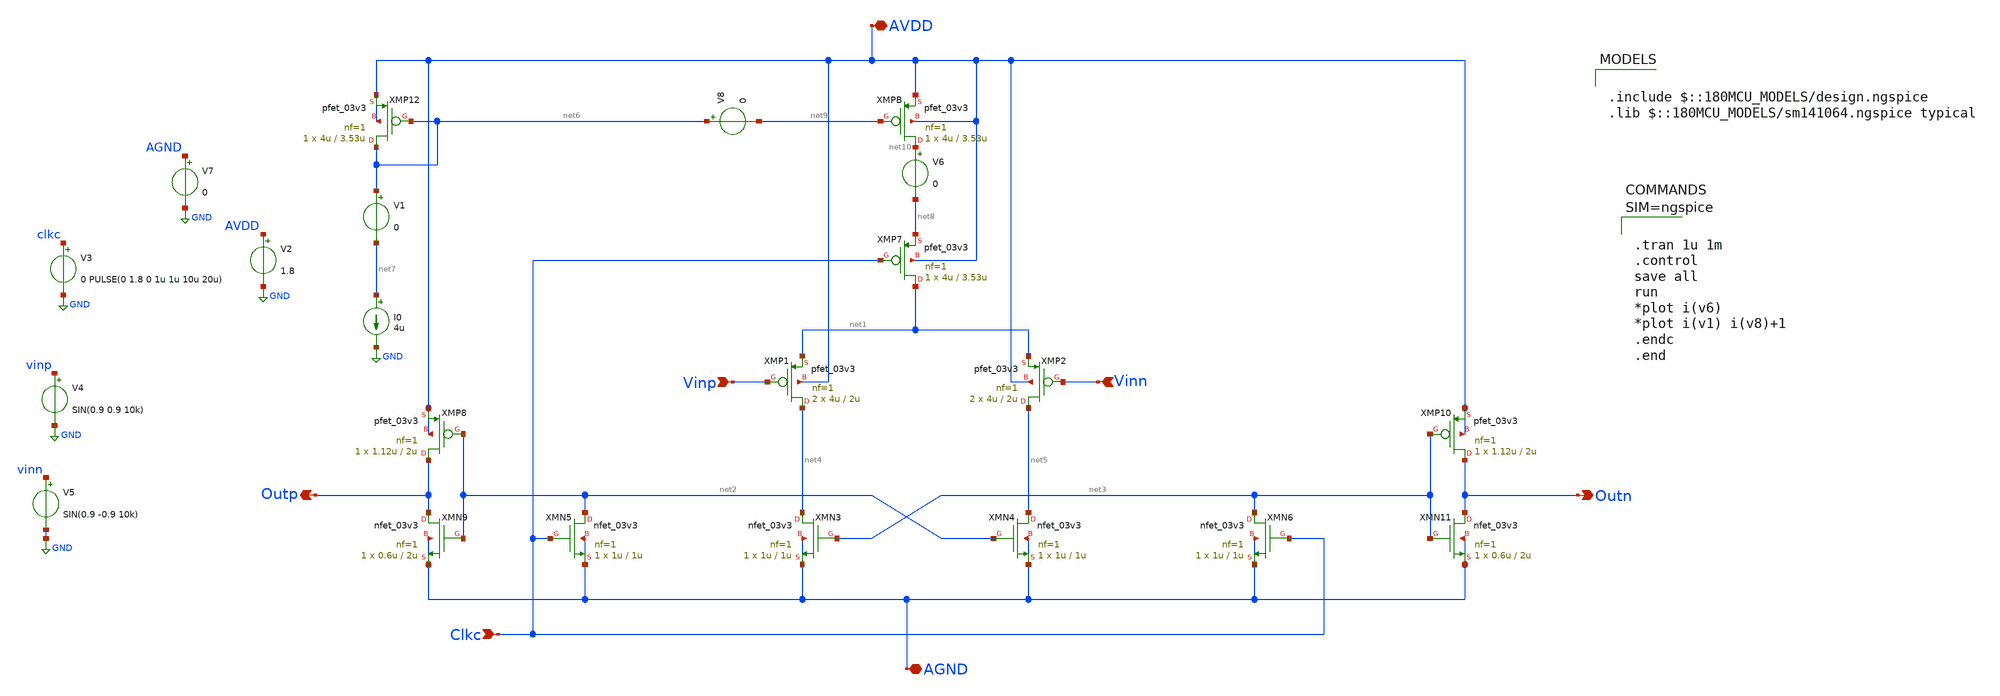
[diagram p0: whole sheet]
** sch_path: xschem/test_dyanamic_comp.sch
**.subckt test_dyanamic_comp AVDD Outp Clkc AGND Outn Vinp Vinn
*.iopin AVDD
*.opin Outp
*.ipin Clkc
*.iopin AGND
*.opin Outn
*.ipin Vinp
*.ipin Vinn
XMP1 net4 Vinp net1 AVDD pfet_03v3 L=2u W=4u nf=1 ad='int((nf+1)/2) * W/nf * 0.18u' as='int((nf+2)/2) * W/nf * 0.18u'
+ pd='2*int((nf+1)/2) * (W/nf + 0.18u)' ps='2*int((nf+2)/2) * (W/nf + 0.18u)' nrd='0.18u / W' nrs='0.18u / W'
+ sa=0 sb=0 sd=0 m=2
XMP2 net5 Vinn net1 AVDD pfet_03v3 L=2u W=4u nf=1 ad='int((nf+1)/2) * W/nf * 0.18u' as='int((nf+2)/2) * W/nf * 0.18u'
+ pd='2*int((nf+1)/2) * (W/nf + 0.18u)' ps='2*int((nf+2)/2) * (W/nf + 0.18u)' nrd='0.18u / W' nrs='0.18u / W'
+ sa=0 sb=0 sd=0 m=2
XMN4 net5 net2 AGND AGND nfet_03v3 L=1u W=1u nf=1 ad='int((nf+1)/2) * W/nf * 0.18u' as='int((nf+2)/2) * W/nf * 0.18u'
+ pd='2*int((nf+1)/2) * (W/nf + 0.18u)' ps='2*int((nf+2)/2) * (W/nf + 0.18u)' nrd='0.18u / W' nrs='0.18u / W'
+ sa=0 sb=0 sd=0 m=1
XMN5 net2 Clkc AGND AGND nfet_03v3 L=1u W=1u nf=1 ad='int((nf+1)/2) * W/nf * 0.18u' as='int((nf+2)/2) * W/nf * 0.18u'
+ pd='2*int((nf+1)/2) * (W/nf + 0.18u)' ps='2*int((nf+2)/2) * (W/nf + 0.18u)' nrd='0.18u / W' nrs='0.18u / W'
+ sa=0 sb=0 sd=0 m=1
XMN6 net3 Clkc AGND AGND nfet_03v3 L=1u W=1u nf=1 ad='int((nf+1)/2) * W/nf * 0.18u' as='int((nf+2)/2) * W/nf * 0.18u'
+ pd='2*int((nf+1)/2) * (W/nf + 0.18u)' ps='2*int((nf+2)/2) * (W/nf + 0.18u)' nrd='0.18u / W' nrs='0.18u / W'
+ sa=0 sb=0 sd=0 m=1
XMN3 net4 net3 AGND AGND nfet_03v3 L=1u W=1u nf=1 ad='int((nf+1)/2) * W/nf * 0.18u' as='int((nf+2)/2) * W/nf * 0.18u'
+ pd='2*int((nf+1)/2) * (W/nf + 0.18u)' ps='2*int((nf+2)/2) * (W/nf + 0.18u)' nrd='0.18u / W' nrs='0.18u / W'
+ sa=0 sb=0 sd=0 m=1
XMP7 net1 Clkc net8 AVDD pfet_03v3 L=3.53u W=4u nf=1 ad='int((nf+1)/2) * W/nf * 0.18u' as='int((nf+2)/2) * W/nf * 0.18u'
+ pd='2*int((nf+1)/2) * (W/nf + 0.18u)' ps='2*int((nf+2)/2) * (W/nf + 0.18u)' nrd='0.18u / W' nrs='0.18u / W'
+ sa=0 sb=0 sd=0 m=1
XMPB net10 net9 AVDD AVDD pfet_03v3 L=3.53u W=4u nf=1 ad='int((nf+1)/2) * W/nf * 0.18u' as='int((nf+2)/2) * W/nf * 0.18u'
+ pd='2*int((nf+1)/2) * (W/nf + 0.18u)' ps='2*int((nf+2)/2) * (W/nf + 0.18u)' nrd='0.18u / W' nrs='0.18u / W'
+ sa=0 sb=0 sd=0 m=1
XMP12 net6 net6 AVDD AVDD pfet_03v3 L=3.53u W=4u nf=1 ad='int((nf+1)/2) * W/nf * 0.18u' as='int((nf+2)/2) * W/nf * 0.18u'
+ pd='2*int((nf+1)/2) * (W/nf + 0.18u)' ps='2*int((nf+2)/2) * (W/nf + 0.18u)' nrd='0.18u / W' nrs='0.18u / W'
+ sa=0 sb=0 sd=0 m=1
XMP10 Outn net3 AVDD AVDD pfet_03v3 L=2u W=1.12u nf=1 ad='int((nf+1)/2) * W/nf * 0.18u' as='int((nf+2)/2) * W/nf * 0.18u'
+ pd='2*int((nf+1)/2) * (W/nf + 0.18u)' ps='2*int((nf+2)/2) * (W/nf + 0.18u)' nrd='0.18u / W' nrs='0.18u / W'
+ sa=0 sb=0 sd=0 m=1
XMN11 Outn net3 AGND AGND nfet_03v3 L=2u W=0.6u nf=1 ad='int((nf+1)/2) * W/nf * 0.18u' as='int((nf+2)/2) * W/nf * 0.18u'
+ pd='2*int((nf+1)/2) * (W/nf + 0.18u)' ps='2*int((nf+2)/2) * (W/nf + 0.18u)' nrd='0.18u / W' nrs='0.18u / W'
+ sa=0 sb=0 sd=0 m=1
XMP8 Outp net2 AVDD AVDD pfet_03v3 L=2u W=1.12u nf=1 ad='int((nf+1)/2) * W/nf * 0.18u' as='int((nf+2)/2) * W/nf * 0.18u'
+ pd='2*int((nf+1)/2) * (W/nf + 0.18u)' ps='2*int((nf+2)/2) * (W/nf + 0.18u)' nrd='0.18u / W' nrs='0.18u / W'
+ sa=0 sb=0 sd=0 m=1
XMN9 Outp net2 AGND AGND nfet_03v3 L=2u W=0.6u nf=1 ad='int((nf+1)/2) * W/nf * 0.18u' as='int((nf+2)/2) * W/nf * 0.18u'
+ pd='2*int((nf+1)/2) * (W/nf + 0.18u)' ps='2*int((nf+2)/2) * (W/nf + 0.18u)' nrd='0.18u / W' nrs='0.18u / W'
+ sa=0 sb=0 sd=0 m=1
V1 net6 net7 0
I0 net7 GND 4u
V2 AVDD GND 1.8
V3 clkc GND 0 PULSE(0 1.8 0 1u 1u 10u 20u)
V4 vinp GND SIN(0.9 0.9 10k)
V5 vinn GND SIN(0.9 -0.9 10k)
V6 net10 net8 0
V7 AGND GND 0
V8 net6 net9 0
**** begin user architecture code

.include $::180MCU_MODELS/design.ngspice
.lib $::180MCU_MODELS/sm141064.ngspice typical




.tran 1u 1m
.control
save all
run
*plot i(v6)
*plot i(v1) i(v8)+1
.endc
.end



**** end user architecture code
**.ends
.GLOBAL GND
.end
